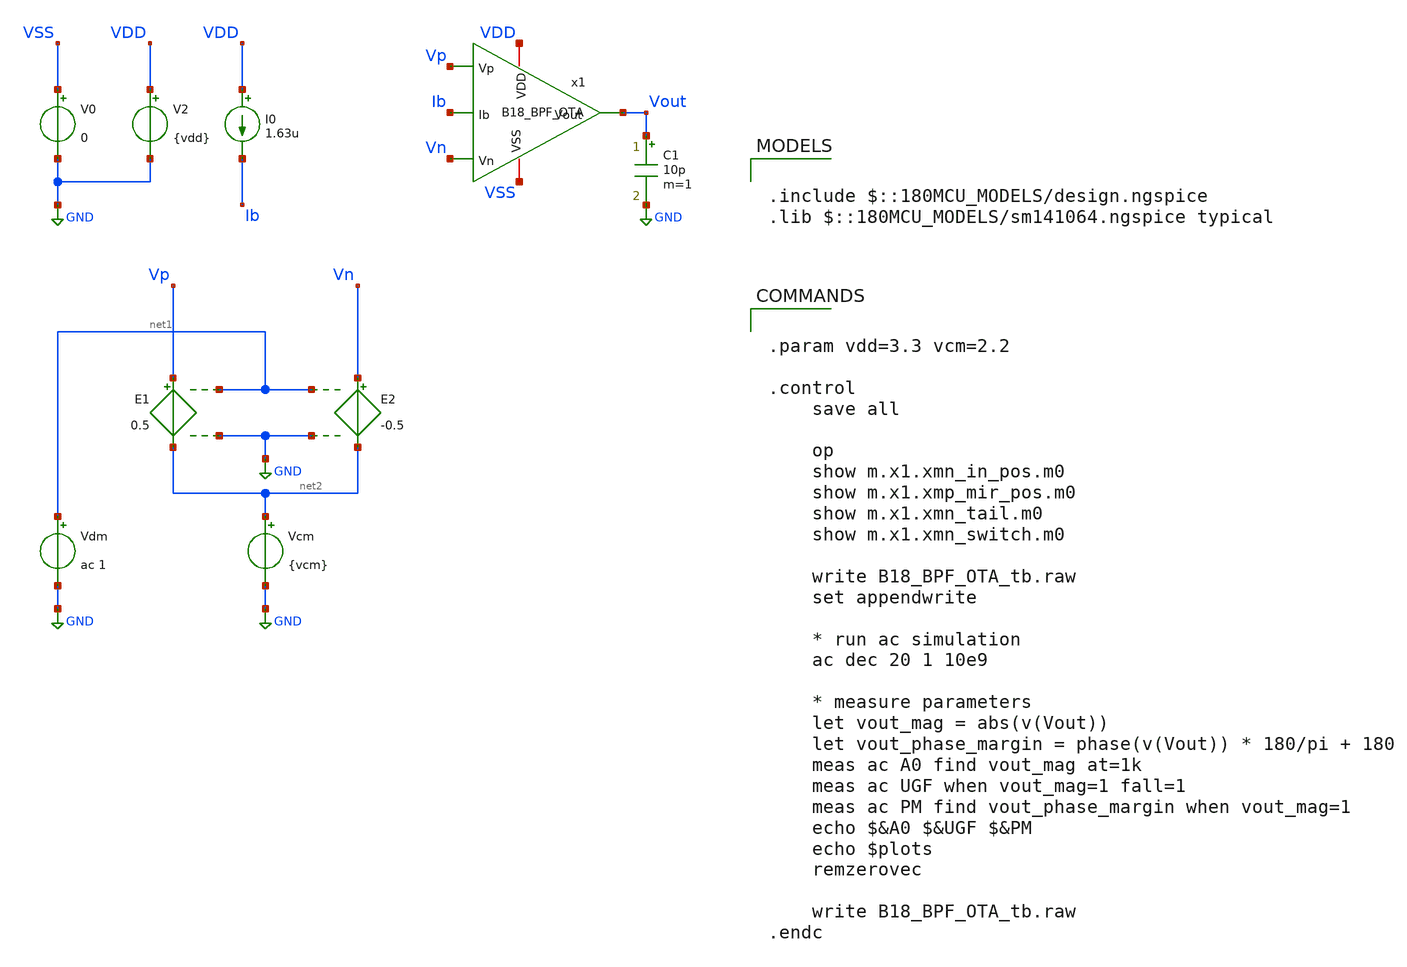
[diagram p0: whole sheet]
** sch_path: Analog/schematics/1_readout/bpf/B18_BPF_OTA_tb.sch
**.subckt B18_BPF_OTA_tb
I0 VDD Ib 1.63u
C1 Vout GND 10p m=1
V0 VSS GND 0
V2 VDD GND {vdd}
E1 Vp net2 net1 GND 0.5
E2 Vn net2 net1 GND -0.5
Vdm net1 GND ac 1
Vcm net2 GND {vcm}
x1 Vp Vn Vout VDD VSS Ib B18_BPF_OTA
**** begin user architecture code


.param vdd=3.3 vcm=2.2

.control
    save all

    op
    show m.x1.xmn_in_pos.m0
    show m.x1.xmp_mir_pos.m0
    show m.x1.xmn_tail.m0
    show m.x1.xmn_switch.m0

    write B18_BPF_OTA_tb.raw
    set appendwrite

    * run ac simulation
    ac dec 20 1 10e9

    * measure parameters
    let vout_mag = abs(v(Vout))
    let vout_phase_margin = phase(v(Vout)) * 180/pi + 180
    meas ac A0 find vout_mag at=1k
    meas ac UGF when vout_mag=1 fall=1
    meas ac PM find vout_phase_margin when vout_mag=1
    echo $&A0 $&UGF $&PM
    echo $plots
    remzerovec

    write B18_BPF_OTA_tb.raw
.endc



.include $::180MCU_MODELS/design.ngspice
.lib $::180MCU_MODELS/sm141064.ngspice typical

**** end user architecture code
**.ends
.GLOBAL GND
.end
